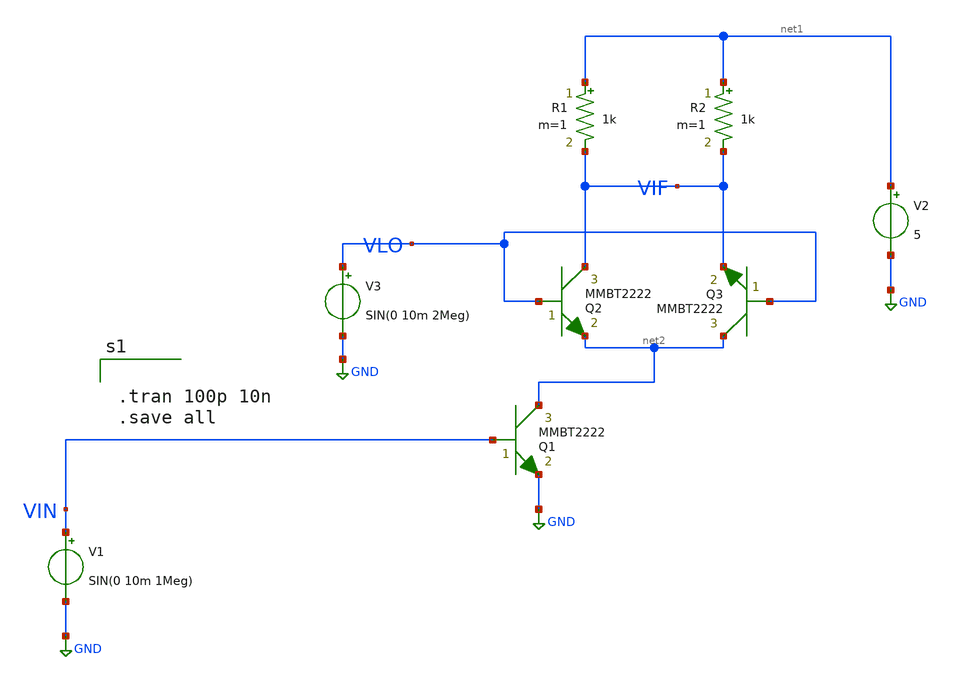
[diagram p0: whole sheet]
** sch_path: mixer/mixer.sch
**.subckt mixer
V1 VIN GND SIN(0 10m 1Meg)
V2 net1 GND 5
R1 net1 VIF 1k m=1
R2 net1 VIF 1k m=1
V3 VLO GND SIN(0 10m 2Meg)
Q1 net2 VIN GND MMBT2222 area=1 m=1
Q2 VIF VLO net2 MMBT2222 area=1 m=1
Q3 net2 VLO VIF MMBT2222 area=1 m=1
**** begin user architecture code


.tran 100p 10n
.save all


**** end user architecture code
**.ends
.GLOBAL GND
.end
